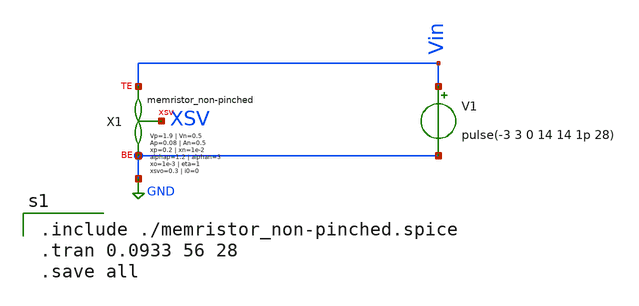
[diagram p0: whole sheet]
** sch_path: apl-paper/ngspice/test_memristor.sch
**.subckt test_memristor
V1 Vin GND pulse(-3 3 0 14 14 1p 28)
X1 GND Vin XSV memristor_non-pinched a1=23.4e-6 a2=0.4e-6 b1=1.1 b2=1.1 Vp=1.9 Vn=0.5 Ap=0.08 An=0.5
+ xp=0.2 xn=1e-2 alphap=1.2 alphan=3 xo=1e-3 eta=1 xsvo=0.3 i0=0 u1=0.72 u2=-0.76 k1=0.2 k2=5.5
**** begin user architecture code

.include ./memristor_non-pinched.spice
.tran 0.0933 56 28
.save all

**** end user architecture code
**.ends

* expanding   symbol:  memristor_non-pinched.sym # of pins=3
** sym_path: apl-paper/ngspice/memristor_non-pinched.sym
.include ./memristor_non-pinched.spice
.GLOBAL GND
.end
